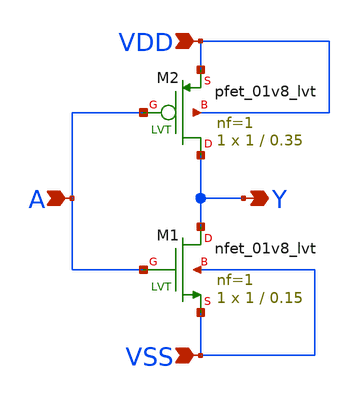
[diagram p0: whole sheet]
** sch_path: xschem/inverter.sch
**.subckt inverter VDD A Y VSS
*.ipin VDD
*.ipin A
*.opin Y
*.ipin VSS
XM2 Y A VDD VDD sky130_fd_pr__pfet_01v8_lvt L=0.35 W=1 nf=1 ad='int((nf+1)/2) * W/nf * 0.29' as='int((nf+2)/2) * W/nf * 0.29'
+ pd='2*int((nf+1)/2) * (W/nf + 0.29)' ps='2*int((nf+2)/2) * (W/nf + 0.29)' nrd='0.29 / W' nrs='0.29 / W'
+ sa=0 sb=0 sd=0 mult=1 m=1
XM1 Y A VSS VSS sky130_fd_pr__nfet_01v8_lvt L=0.15 W=1 nf=1 ad='int((nf+1)/2) * W/nf * 0.29' as='int((nf+2)/2) * W/nf * 0.29'
+ pd='2*int((nf+1)/2) * (W/nf + 0.29)' ps='2*int((nf+2)/2) * (W/nf + 0.29)' nrd='0.29 / W' nrs='0.29 / W'
+ sa=0 sb=0 sd=0 mult=1 m=1
**.ends
.end
